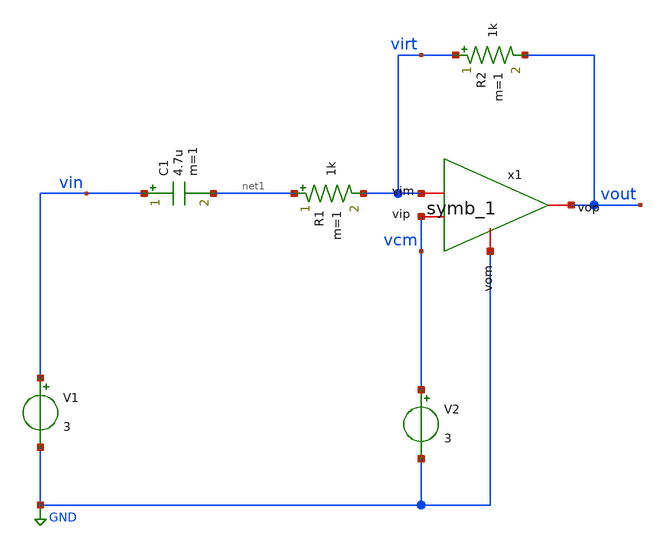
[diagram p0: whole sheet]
** sch_path: xschem/untitled.sch
**.subckt untitled
x1 vout vcm virt GND symb_1
R1 net1 virt 1k m=1
R2 virt vout 1k m=1
C1 vin net1 4.7u m=1
V1 vin GND 3
V2 vcm GND 3
**.ends

* expanding   symbol:  symb_1.sym # of pins=4
** sym_path: xschem/symb_1.sym
** sch_path: xschem/symb_1.sch
.subckt symb_1 vop vip vim vom
*.iopin vip
*.iopin vim
*.iopin vop
*.iopin vom
E1 vop vom vip vim 3
.ends

.GLOBAL GND
.end
